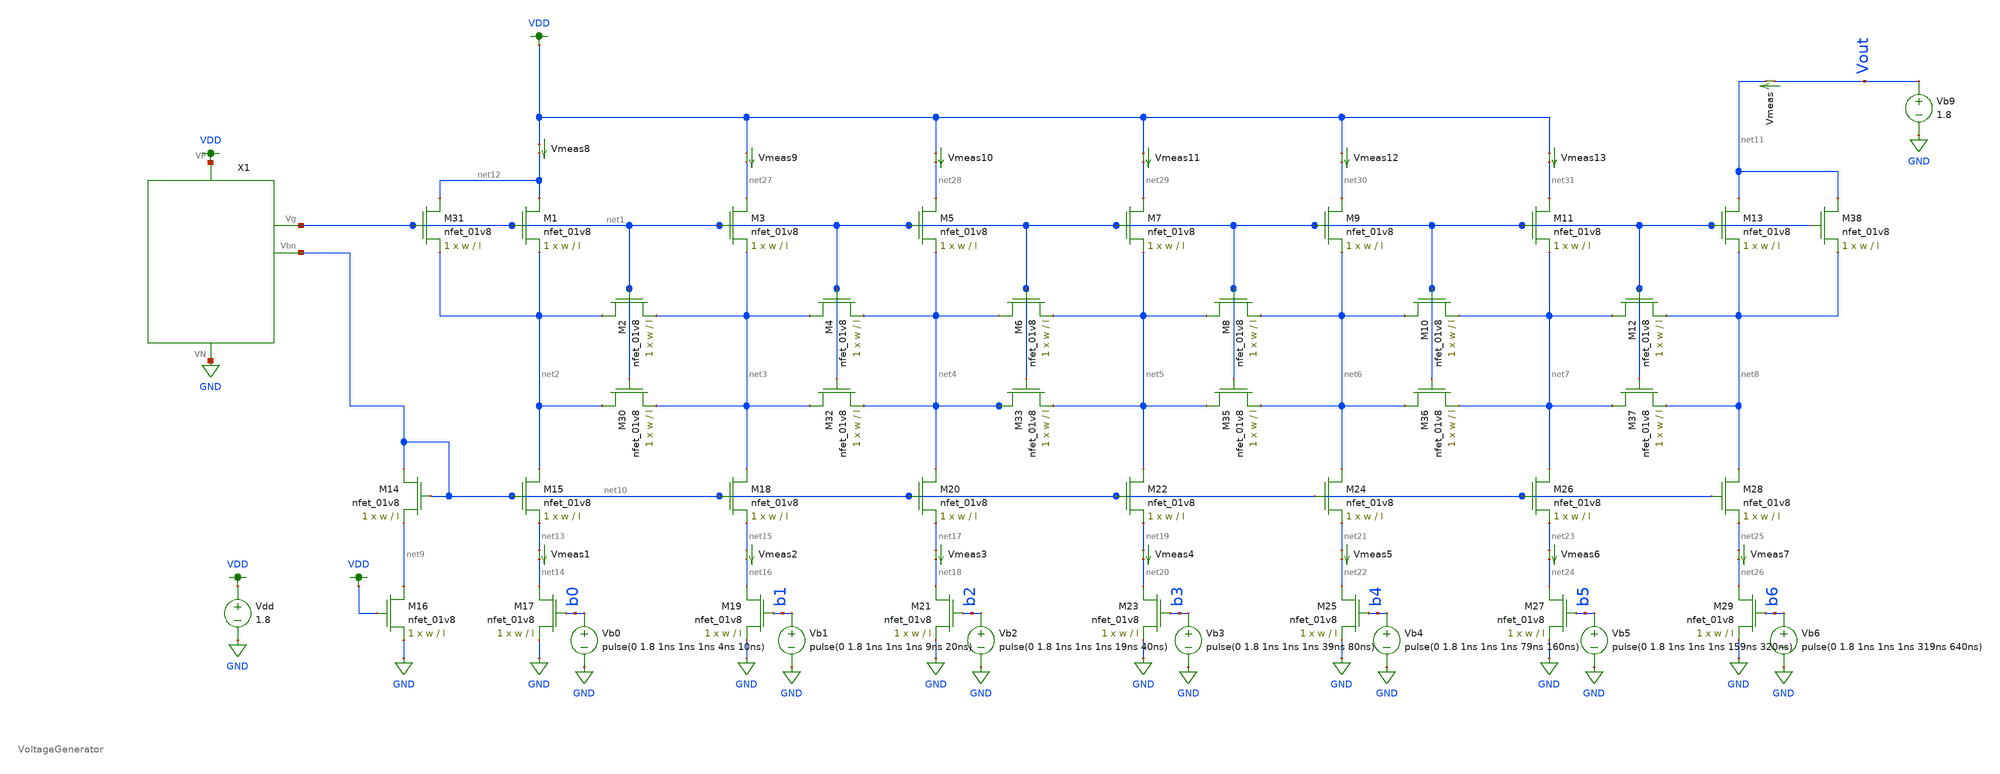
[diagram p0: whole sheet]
** sch_path: DAC_dnl_vsource.sch
**.subckt DAC_dnl_vsource
XM1 net12 net1 net2 GND sky130_fd_pr__nfet_01v8 L=l W=w nf=1 ad='int((nf+1)/2) * W/nf * 0.29' as='int((nf+2)/2) * W/nf * 0.29'
+ pd='2*int((nf+1)/2) * (W/nf + 0.29)' ps='2*int((nf+2)/2) * (W/nf + 0.29)' nrd='0.29 / W' nrs='0.29 / W'
+ sa=0 sb=0 sd=0 mult=1 m=1
XM2 net2 net1 net3 GND sky130_fd_pr__nfet_01v8 L=l W=w nf=1 ad='int((nf+1)/2) * W/nf * 0.29' as='int((nf+2)/2) * W/nf * 0.29'
+ pd='2*int((nf+1)/2) * (W/nf + 0.29)' ps='2*int((nf+2)/2) * (W/nf + 0.29)' nrd='0.29 / W' nrs='0.29 / W'
+ sa=0 sb=0 sd=0 mult=1 m=1
XM3 net27 net1 net3 GND sky130_fd_pr__nfet_01v8 L=l W=w nf=1 ad='int((nf+1)/2) * W/nf * 0.29' as='int((nf+2)/2) * W/nf * 0.29'
+ pd='2*int((nf+1)/2) * (W/nf + 0.29)' ps='2*int((nf+2)/2) * (W/nf + 0.29)' nrd='0.29 / W' nrs='0.29 / W'
+ sa=0 sb=0 sd=0 mult=1 m=1
XM4 net3 net1 net4 GND sky130_fd_pr__nfet_01v8 L=l W=w nf=1 ad='int((nf+1)/2) * W/nf * 0.29' as='int((nf+2)/2) * W/nf * 0.29'
+ pd='2*int((nf+1)/2) * (W/nf + 0.29)' ps='2*int((nf+2)/2) * (W/nf + 0.29)' nrd='0.29 / W' nrs='0.29 / W'
+ sa=0 sb=0 sd=0 mult=1 m=1
XM5 net28 net1 net4 GND sky130_fd_pr__nfet_01v8 L=l W=w nf=1 ad='int((nf+1)/2) * W/nf * 0.29' as='int((nf+2)/2) * W/nf * 0.29'
+ pd='2*int((nf+1)/2) * (W/nf + 0.29)' ps='2*int((nf+2)/2) * (W/nf + 0.29)' nrd='0.29 / W' nrs='0.29 / W'
+ sa=0 sb=0 sd=0 mult=1 m=1
XM6 net4 net1 net5 GND sky130_fd_pr__nfet_01v8 L=l W=w nf=1 ad='int((nf+1)/2) * W/nf * 0.29' as='int((nf+2)/2) * W/nf * 0.29'
+ pd='2*int((nf+1)/2) * (W/nf + 0.29)' ps='2*int((nf+2)/2) * (W/nf + 0.29)' nrd='0.29 / W' nrs='0.29 / W'
+ sa=0 sb=0 sd=0 mult=1 m=1
XM7 net29 net1 net5 GND sky130_fd_pr__nfet_01v8 L=l W=w nf=1 ad='int((nf+1)/2) * W/nf * 0.29' as='int((nf+2)/2) * W/nf * 0.29'
+ pd='2*int((nf+1)/2) * (W/nf + 0.29)' ps='2*int((nf+2)/2) * (W/nf + 0.29)' nrd='0.29 / W' nrs='0.29 / W'
+ sa=0 sb=0 sd=0 mult=1 m=1
XM8 net5 net1 net6 GND sky130_fd_pr__nfet_01v8 L=l W=w nf=1 ad='int((nf+1)/2) * W/nf * 0.29' as='int((nf+2)/2) * W/nf * 0.29'
+ pd='2*int((nf+1)/2) * (W/nf + 0.29)' ps='2*int((nf+2)/2) * (W/nf + 0.29)' nrd='0.29 / W' nrs='0.29 / W'
+ sa=0 sb=0 sd=0 mult=1 m=1
XM9 net30 net1 net6 GND sky130_fd_pr__nfet_01v8 L=l W=w nf=1 ad='int((nf+1)/2) * W/nf * 0.29' as='int((nf+2)/2) * W/nf * 0.29'
+ pd='2*int((nf+1)/2) * (W/nf + 0.29)' ps='2*int((nf+2)/2) * (W/nf + 0.29)' nrd='0.29 / W' nrs='0.29 / W'
+ sa=0 sb=0 sd=0 mult=1 m=1
XM10 net6 net1 net7 GND sky130_fd_pr__nfet_01v8 L=l W=w nf=1 ad='int((nf+1)/2) * W/nf * 0.29' as='int((nf+2)/2) * W/nf * 0.29'
+ pd='2*int((nf+1)/2) * (W/nf + 0.29)' ps='2*int((nf+2)/2) * (W/nf + 0.29)' nrd='0.29 / W' nrs='0.29 / W'
+ sa=0 sb=0 sd=0 mult=1 m=1
XM11 net31 net1 net7 GND sky130_fd_pr__nfet_01v8 L=l W=w nf=1 ad='int((nf+1)/2) * W/nf * 0.29' as='int((nf+2)/2) * W/nf * 0.29'
+ pd='2*int((nf+1)/2) * (W/nf + 0.29)' ps='2*int((nf+2)/2) * (W/nf + 0.29)' nrd='0.29 / W' nrs='0.29 / W'
+ sa=0 sb=0 sd=0 mult=1 m=1
XM12 net7 net1 net8 GND sky130_fd_pr__nfet_01v8 L=l W=w nf=1 ad='int((nf+1)/2) * W/nf * 0.29' as='int((nf+2)/2) * W/nf * 0.29'
+ pd='2*int((nf+1)/2) * (W/nf + 0.29)' ps='2*int((nf+2)/2) * (W/nf + 0.29)' nrd='0.29 / W' nrs='0.29 / W'
+ sa=0 sb=0 sd=0 mult=1 m=1
XM13 net11 net1 net8 GND sky130_fd_pr__nfet_01v8 L=l W=w nf=1 ad='int((nf+1)/2) * W/nf * 0.29' as='int((nf+2)/2) * W/nf * 0.29'
+ pd='2*int((nf+1)/2) * (W/nf + 0.29)' ps='2*int((nf+2)/2) * (W/nf + 0.29)' nrd='0.29 / W' nrs='0.29 / W'
+ sa=0 sb=0 sd=0 mult=1 m=1
XM14 net10 net10 net9 GND sky130_fd_pr__nfet_01v8 L=l W=w nf=1 ad='int((nf+1)/2) * W/nf * 0.29' as='int((nf+2)/2) * W/nf * 0.29'
+ pd='2*int((nf+1)/2) * (W/nf + 0.29)' ps='2*int((nf+2)/2) * (W/nf + 0.29)' nrd='0.29 / W' nrs='0.29 / W'
+ sa=0 sb=0 sd=0 mult=1 m=1
XM15 net2 net10 net13 GND sky130_fd_pr__nfet_01v8 L=l W=w nf=1 ad='int((nf+1)/2) * W/nf * 0.29' as='int((nf+2)/2) * W/nf * 0.29'
+ pd='2*int((nf+1)/2) * (W/nf + 0.29)' ps='2*int((nf+2)/2) * (W/nf + 0.29)' nrd='0.29 / W' nrs='0.29 / W'
+ sa=0 sb=0 sd=0 mult=1 m=1
XM16 net9 VDD GND GND sky130_fd_pr__nfet_01v8 L=l W=w nf=1 ad='int((nf+1)/2) * W/nf * 0.29' as='int((nf+2)/2) * W/nf * 0.29'
+ pd='2*int((nf+1)/2) * (W/nf + 0.29)' ps='2*int((nf+2)/2) * (W/nf + 0.29)' nrd='0.29 / W' nrs='0.29 / W'
+ sa=0 sb=0 sd=0 mult=1 m=1
XM17 net14 b0 GND GND sky130_fd_pr__nfet_01v8 L=l W=w nf=1 ad='int((nf+1)/2) * W/nf * 0.29' as='int((nf+2)/2) * W/nf * 0.29'
+ pd='2*int((nf+1)/2) * (W/nf + 0.29)' ps='2*int((nf+2)/2) * (W/nf + 0.29)' nrd='0.29 / W' nrs='0.29 / W'
+ sa=0 sb=0 sd=0 mult=1 m=1
XM18 net3 net10 net15 GND sky130_fd_pr__nfet_01v8 L=l W=w nf=1 ad='int((nf+1)/2) * W/nf * 0.29' as='int((nf+2)/2) * W/nf * 0.29'
+ pd='2*int((nf+1)/2) * (W/nf + 0.29)' ps='2*int((nf+2)/2) * (W/nf + 0.29)' nrd='0.29 / W' nrs='0.29 / W'
+ sa=0 sb=0 sd=0 mult=1 m=1
XM19 net16 b1 GND GND sky130_fd_pr__nfet_01v8 L=l W=w nf=1 ad='int((nf+1)/2) * W/nf * 0.29' as='int((nf+2)/2) * W/nf * 0.29'
+ pd='2*int((nf+1)/2) * (W/nf + 0.29)' ps='2*int((nf+2)/2) * (W/nf + 0.29)' nrd='0.29 / W' nrs='0.29 / W'
+ sa=0 sb=0 sd=0 mult=1 m=1
XM20 net4 net10 net17 GND sky130_fd_pr__nfet_01v8 L=l W=w nf=1 ad='int((nf+1)/2) * W/nf * 0.29' as='int((nf+2)/2) * W/nf * 0.29'
+ pd='2*int((nf+1)/2) * (W/nf + 0.29)' ps='2*int((nf+2)/2) * (W/nf + 0.29)' nrd='0.29 / W' nrs='0.29 / W'
+ sa=0 sb=0 sd=0 mult=1 m=1
XM21 net18 b2 GND GND sky130_fd_pr__nfet_01v8 L=l W=w nf=1 ad='int((nf+1)/2) * W/nf * 0.29' as='int((nf+2)/2) * W/nf * 0.29'
+ pd='2*int((nf+1)/2) * (W/nf + 0.29)' ps='2*int((nf+2)/2) * (W/nf + 0.29)' nrd='0.29 / W' nrs='0.29 / W'
+ sa=0 sb=0 sd=0 mult=1 m=1
XM22 net5 net10 net19 GND sky130_fd_pr__nfet_01v8 L=l W=w nf=1 ad='int((nf+1)/2) * W/nf * 0.29' as='int((nf+2)/2) * W/nf * 0.29'
+ pd='2*int((nf+1)/2) * (W/nf + 0.29)' ps='2*int((nf+2)/2) * (W/nf + 0.29)' nrd='0.29 / W' nrs='0.29 / W'
+ sa=0 sb=0 sd=0 mult=1 m=1
XM23 net20 b3 GND GND sky130_fd_pr__nfet_01v8 L=l W=w nf=1 ad='int((nf+1)/2) * W/nf * 0.29' as='int((nf+2)/2) * W/nf * 0.29'
+ pd='2*int((nf+1)/2) * (W/nf + 0.29)' ps='2*int((nf+2)/2) * (W/nf + 0.29)' nrd='0.29 / W' nrs='0.29 / W'
+ sa=0 sb=0 sd=0 mult=1 m=1
XM24 net6 net10 net21 GND sky130_fd_pr__nfet_01v8 L=l W=w nf=1 ad='int((nf+1)/2) * W/nf * 0.29' as='int((nf+2)/2) * W/nf * 0.29'
+ pd='2*int((nf+1)/2) * (W/nf + 0.29)' ps='2*int((nf+2)/2) * (W/nf + 0.29)' nrd='0.29 / W' nrs='0.29 / W'
+ sa=0 sb=0 sd=0 mult=1 m=1
XM25 net22 b4 GND GND sky130_fd_pr__nfet_01v8 L=l W=w nf=1 ad='int((nf+1)/2) * W/nf * 0.29' as='int((nf+2)/2) * W/nf * 0.29'
+ pd='2*int((nf+1)/2) * (W/nf + 0.29)' ps='2*int((nf+2)/2) * (W/nf + 0.29)' nrd='0.29 / W' nrs='0.29 / W'
+ sa=0 sb=0 sd=0 mult=1 m=1
XM26 net7 net10 net23 GND sky130_fd_pr__nfet_01v8 L=l W=w nf=1 ad='int((nf+1)/2) * W/nf * 0.29' as='int((nf+2)/2) * W/nf * 0.29'
+ pd='2*int((nf+1)/2) * (W/nf + 0.29)' ps='2*int((nf+2)/2) * (W/nf + 0.29)' nrd='0.29 / W' nrs='0.29 / W'
+ sa=0 sb=0 sd=0 mult=1 m=1
XM27 net24 b5 GND GND sky130_fd_pr__nfet_01v8 L=l W=w nf=1 ad='int((nf+1)/2) * W/nf * 0.29' as='int((nf+2)/2) * W/nf * 0.29'
+ pd='2*int((nf+1)/2) * (W/nf + 0.29)' ps='2*int((nf+2)/2) * (W/nf + 0.29)' nrd='0.29 / W' nrs='0.29 / W'
+ sa=0 sb=0 sd=0 mult=1 m=1
XM28 net8 net10 net25 GND sky130_fd_pr__nfet_01v8 L=l W=w nf=1 ad='int((nf+1)/2) * W/nf * 0.29' as='int((nf+2)/2) * W/nf * 0.29'
+ pd='2*int((nf+1)/2) * (W/nf + 0.29)' ps='2*int((nf+2)/2) * (W/nf + 0.29)' nrd='0.29 / W' nrs='0.29 / W'
+ sa=0 sb=0 sd=0 mult=1 m=1
XM29 net26 b6 GND GND sky130_fd_pr__nfet_01v8 L=l W=w nf=1 ad='int((nf+1)/2) * W/nf * 0.29' as='int((nf+2)/2) * W/nf * 0.29'
+ pd='2*int((nf+1)/2) * (W/nf + 0.29)' ps='2*int((nf+2)/2) * (W/nf + 0.29)' nrd='0.29 / W' nrs='0.29 / W'
+ sa=0 sb=0 sd=0 mult=1 m=1
XM30 net2 net1 net3 GND sky130_fd_pr__nfet_01v8 L=l W=w nf=1 ad='int((nf+1)/2) * W/nf * 0.29' as='int((nf+2)/2) * W/nf * 0.29'
+ pd='2*int((nf+1)/2) * (W/nf + 0.29)' ps='2*int((nf+2)/2) * (W/nf + 0.29)' nrd='0.29 / W' nrs='0.29 / W'
+ sa=0 sb=0 sd=0 mult=1 m=1
XM31 net12 net1 net2 GND sky130_fd_pr__nfet_01v8 L=l W=w nf=1 ad='int((nf+1)/2) * W/nf * 0.29' as='int((nf+2)/2) * W/nf * 0.29'
+ pd='2*int((nf+1)/2) * (W/nf + 0.29)' ps='2*int((nf+2)/2) * (W/nf + 0.29)' nrd='0.29 / W' nrs='0.29 / W'
+ sa=0 sb=0 sd=0 mult=1 m=1
XM32 net3 net1 net4 GND sky130_fd_pr__nfet_01v8 L=l W=w nf=1 ad='int((nf+1)/2) * W/nf * 0.29' as='int((nf+2)/2) * W/nf * 0.29'
+ pd='2*int((nf+1)/2) * (W/nf + 0.29)' ps='2*int((nf+2)/2) * (W/nf + 0.29)' nrd='0.29 / W' nrs='0.29 / W'
+ sa=0 sb=0 sd=0 mult=1 m=1
XM33 net4 net1 net5 GND sky130_fd_pr__nfet_01v8 L=l W=w nf=1 ad='int((nf+1)/2) * W/nf * 0.29' as='int((nf+2)/2) * W/nf * 0.29'
+ pd='2*int((nf+1)/2) * (W/nf + 0.29)' ps='2*int((nf+2)/2) * (W/nf + 0.29)' nrd='0.29 / W' nrs='0.29 / W'
+ sa=0 sb=0 sd=0 mult=1 m=1
XM35 net5 net1 net6 GND sky130_fd_pr__nfet_01v8 L=l W=w nf=1 ad='int((nf+1)/2) * W/nf * 0.29' as='int((nf+2)/2) * W/nf * 0.29'
+ pd='2*int((nf+1)/2) * (W/nf + 0.29)' ps='2*int((nf+2)/2) * (W/nf + 0.29)' nrd='0.29 / W' nrs='0.29 / W'
+ sa=0 sb=0 sd=0 mult=1 m=1
XM36 net6 net1 net7 GND sky130_fd_pr__nfet_01v8 L=l W=w nf=1 ad='int((nf+1)/2) * W/nf * 0.29' as='int((nf+2)/2) * W/nf * 0.29'
+ pd='2*int((nf+1)/2) * (W/nf + 0.29)' ps='2*int((nf+2)/2) * (W/nf + 0.29)' nrd='0.29 / W' nrs='0.29 / W'
+ sa=0 sb=0 sd=0 mult=1 m=1
XM37 net7 net1 net8 GND sky130_fd_pr__nfet_01v8 L=l W=w nf=1 ad='int((nf+1)/2) * W/nf * 0.29' as='int((nf+2)/2) * W/nf * 0.29'
+ pd='2*int((nf+1)/2) * (W/nf + 0.29)' ps='2*int((nf+2)/2) * (W/nf + 0.29)' nrd='0.29 / W' nrs='0.29 / W'
+ sa=0 sb=0 sd=0 mult=1 m=1
XM38 net11 net1 net8 GND sky130_fd_pr__nfet_01v8 L=l W=w nf=1 ad='int((nf+1)/2) * W/nf * 0.29' as='int((nf+2)/2) * W/nf * 0.29'
+ pd='2*int((nf+1)/2) * (W/nf + 0.29)' ps='2*int((nf+2)/2) * (W/nf + 0.29)' nrd='0.29 / W' nrs='0.29 / W'
+ sa=0 sb=0 sd=0 mult=1 m=1
X1 GND VDD net1 net10 VoltageGenerator
Vmeas Vout net11 0
.save i(vmeas)
Vb0 b0 GND pulse(0 1.8 1ns 1ns 1ns 4ns 10ns)
Vb1 b1 GND pulse(0 1.8 1ns 1ns 1ns 9ns 20ns)
Vb2 b2 GND pulse(0 1.8 1ns 1ns 1ns 19ns 40ns)
Vb3 b3 GND pulse(0 1.8 1ns 1ns 1ns 39ns 80ns)
Vb4 b4 GND pulse(0 1.8 1ns 1ns 1ns 79ns 160ns)
Vb5 b5 GND pulse(0 1.8 1ns 1ns 1ns 159ns 320ns)
Vb6 b6 GND pulse(0 1.8 1ns 1ns 1ns 319ns 640ns)
Vdd VDD GND 1.8
Vb9 Vout GND 1.8
Vmeas1 net13 net14 0
.save i(vmeas1)
Vmeas2 net15 net16 0
.save i(vmeas2)
Vmeas3 net17 net18 0
.save i(vmeas3)
Vmeas4 net19 net20 0
.save i(vmeas4)
Vmeas5 net21 net22 0
.save i(vmeas5)
Vmeas6 net23 net24 0
.save i(vmeas6)
Vmeas7 net25 net26 0
.save i(vmeas7)
Vmeas8 VDD net12 0
.save i(vmeas8)
Vmeas9 VDD net27 0
.save i(vmeas9)
Vmeas10 VDD net28 0
.save i(vmeas10)
Vmeas11 VDD net29 0
.save i(vmeas11)
Vmeas12 VDD net30 0
.save i(vmeas12)
Vmeas13 VDD net31 0
.save i(vmeas13)
**** begin user architecture code

.tran 0.01n 650n
.param w = 4
.param l = 10
.save all


.option wnflag=1
.param MC_SWITCH=0.0
.lib ~/skywater/skywater-pdk/libraries/sky130_fd_pr_ngspice/latest/models/sky130.lib.spice tt

**** end user architecture code
**.ends
.GLOBAL GND
.GLOBAL VDD
.end
